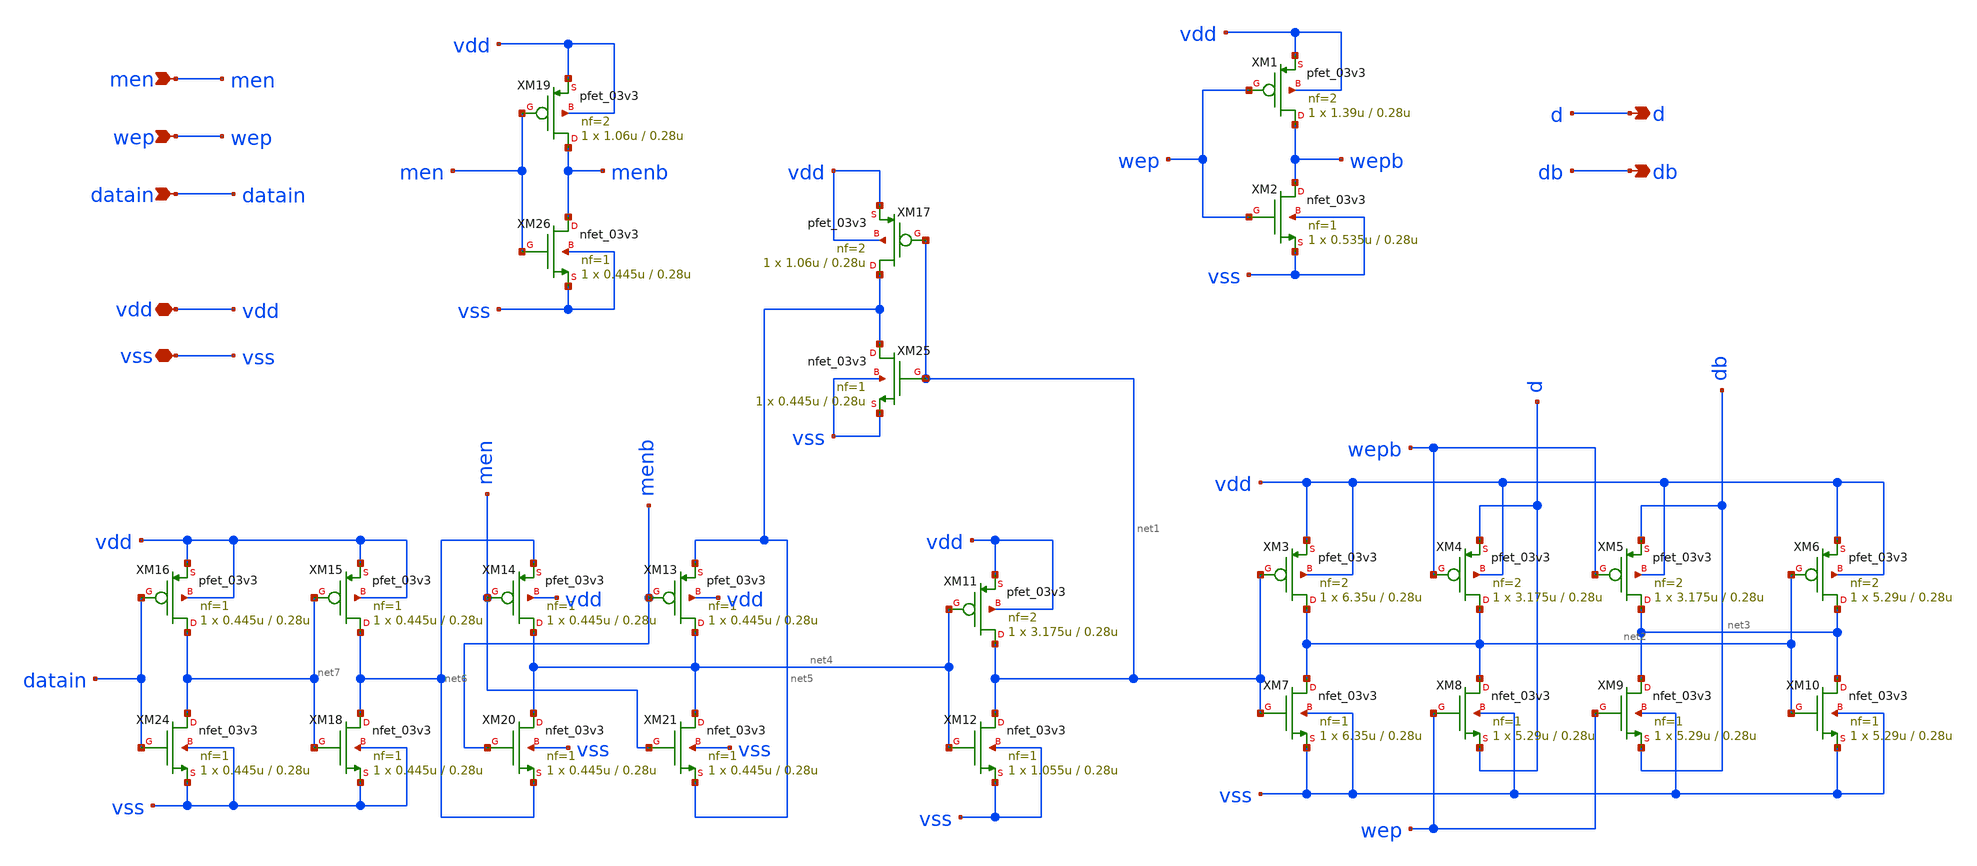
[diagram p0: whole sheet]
** sch_path: cells/gf180mcu_ocd_ip_sram__sram512x8m8wm1/xschem/din_3v512x8m81.sch
**.subckt din_3v512x8m81 men wep datain d db vdd vss
*.ipin men
*.ipin wep
*.ipin datain
*.opin d
*.opin db
*.iopin vdd
*.iopin vss
XM1 wepb wep vdd vdd pfet_03v3 L=0.28u W=1.39u nf=2 ad='int((nf+1)/2) * W/nf * 0.18u' as='int((nf+2)/2) * W/nf * 0.18u'
+ pd='2*int((nf+1)/2) * (W/nf + 0.18u)' ps='2*int((nf+2)/2) * (W/nf + 0.18u)' nrd='0.18u / W' nrs='0.18u / W'
+ sa=0 sb=0 sd=0 m=1
XM2 wepb wep vss vss nfet_03v3 L=0.28u W=0.535u nf=1 ad='int((nf+1)/2) * W/nf * 0.18u' as='int((nf+2)/2) * W/nf * 0.18u'
+ pd='2*int((nf+1)/2) * (W/nf + 0.18u)' ps='2*int((nf+2)/2) * (W/nf + 0.18u)' nrd='0.18u / W' nrs='0.18u / W'
+ sa=0 sb=0 sd=0 m=1
XM3 net2 net1 vdd vdd pfet_03v3 L=0.28u W=6.35u nf=2 ad='int((nf+1)/2) * W/nf * 0.18u' as='int((nf+2)/2) * W/nf * 0.18u'
+ pd='2*int((nf+1)/2) * (W/nf + 0.18u)' ps='2*int((nf+2)/2) * (W/nf + 0.18u)' nrd='0.18u / W' nrs='0.18u / W'
+ sa=0 sb=0 sd=0 m=1
XM4 net2 wepb d vdd pfet_03v3 L=0.28u W=3.175u nf=2 ad='int((nf+1)/2) * W/nf * 0.18u' as='int((nf+2)/2) * W/nf * 0.18u'
+ pd='2*int((nf+1)/2) * (W/nf + 0.18u)' ps='2*int((nf+2)/2) * (W/nf + 0.18u)' nrd='0.18u / W' nrs='0.18u / W'
+ sa=0 sb=0 sd=0 m=1
XM5 net3 wepb db vdd pfet_03v3 L=0.28u W=3.175u nf=2 ad='int((nf+1)/2) * W/nf * 0.18u' as='int((nf+2)/2) * W/nf * 0.18u'
+ pd='2*int((nf+1)/2) * (W/nf + 0.18u)' ps='2*int((nf+2)/2) * (W/nf + 0.18u)' nrd='0.18u / W' nrs='0.18u / W'
+ sa=0 sb=0 sd=0 m=1
XM6 net3 net2 vdd vdd pfet_03v3 L=0.28u W=5.29u nf=2 ad='int((nf+1)/2) * W/nf * 0.18u' as='int((nf+2)/2) * W/nf * 0.18u'
+ pd='2*int((nf+1)/2) * (W/nf + 0.18u)' ps='2*int((nf+2)/2) * (W/nf + 0.18u)' nrd='0.18u / W' nrs='0.18u / W'
+ sa=0 sb=0 sd=0 m=1
XM7 net2 net1 vss vss nfet_03v3 L=0.28u W=6.35u nf=1 ad='int((nf+1)/2) * W/nf * 0.18u' as='int((nf+2)/2) * W/nf * 0.18u'
+ pd='2*int((nf+1)/2) * (W/nf + 0.18u)' ps='2*int((nf+2)/2) * (W/nf + 0.18u)' nrd='0.18u / W' nrs='0.18u / W'
+ sa=0 sb=0 sd=0 m=1
XM8 net2 wep d vss nfet_03v3 L=0.28u W=5.29u nf=1 ad='int((nf+1)/2) * W/nf * 0.18u' as='int((nf+2)/2) * W/nf * 0.18u'
+ pd='2*int((nf+1)/2) * (W/nf + 0.18u)' ps='2*int((nf+2)/2) * (W/nf + 0.18u)' nrd='0.18u / W' nrs='0.18u / W'
+ sa=0 sb=0 sd=0 m=1
XM9 net3 wep db vss nfet_03v3 L=0.28u W=5.29u nf=1 ad='int((nf+1)/2) * W/nf * 0.18u' as='int((nf+2)/2) * W/nf * 0.18u'
+ pd='2*int((nf+1)/2) * (W/nf + 0.18u)' ps='2*int((nf+2)/2) * (W/nf + 0.18u)' nrd='0.18u / W' nrs='0.18u / W'
+ sa=0 sb=0 sd=0 m=1
XM10 net3 net2 vss vss nfet_03v3 L=0.28u W=5.29u nf=1 ad='int((nf+1)/2) * W/nf * 0.18u' as='int((nf+2)/2) * W/nf * 0.18u'
+ pd='2*int((nf+1)/2) * (W/nf + 0.18u)' ps='2*int((nf+2)/2) * (W/nf + 0.18u)' nrd='0.18u / W' nrs='0.18u / W'
+ sa=0 sb=0 sd=0 m=1
XM11 net1 net4 vdd vdd pfet_03v3 L=0.28u W=3.175u nf=2 ad='int((nf+1)/2) * W/nf * 0.18u' as='int((nf+2)/2) * W/nf * 0.18u'
+ pd='2*int((nf+1)/2) * (W/nf + 0.18u)' ps='2*int((nf+2)/2) * (W/nf + 0.18u)' nrd='0.18u / W' nrs='0.18u / W'
+ sa=0 sb=0 sd=0 m=1
XM12 net1 net4 vss vss nfet_03v3 L=0.28u W=1.055u nf=1 ad='int((nf+1)/2) * W/nf * 0.18u' as='int((nf+2)/2) * W/nf * 0.18u'
+ pd='2*int((nf+1)/2) * (W/nf + 0.18u)' ps='2*int((nf+2)/2) * (W/nf + 0.18u)' nrd='0.18u / W' nrs='0.18u / W'
+ sa=0 sb=0 sd=0 m=1
XM13 net4 menb net5 vdd pfet_03v3 L=0.28u W=0.445u nf=1 ad='int((nf+1)/2) * W/nf * 0.18u' as='int((nf+2)/2) * W/nf * 0.18u'
+ pd='2*int((nf+1)/2) * (W/nf + 0.18u)' ps='2*int((nf+2)/2) * (W/nf + 0.18u)' nrd='0.18u / W' nrs='0.18u / W'
+ sa=0 sb=0 sd=0 m=1
XM14 net4 men net6 vdd pfet_03v3 L=0.28u W=0.445u nf=1 ad='int((nf+1)/2) * W/nf * 0.18u' as='int((nf+2)/2) * W/nf * 0.18u'
+ pd='2*int((nf+1)/2) * (W/nf + 0.18u)' ps='2*int((nf+2)/2) * (W/nf + 0.18u)' nrd='0.18u / W' nrs='0.18u / W'
+ sa=0 sb=0 sd=0 m=1
XM15 net6 net7 vdd vdd pfet_03v3 L=0.28u W=0.445u nf=1 ad='int((nf+1)/2) * W/nf * 0.18u' as='int((nf+2)/2) * W/nf * 0.18u'
+ pd='2*int((nf+1)/2) * (W/nf + 0.18u)' ps='2*int((nf+2)/2) * (W/nf + 0.18u)' nrd='0.18u / W' nrs='0.18u / W'
+ sa=0 sb=0 sd=0 m=1
XM16 net7 datain vdd vdd pfet_03v3 L=0.28u W=0.445u nf=1 ad='int((nf+1)/2) * W/nf * 0.18u' as='int((nf+2)/2) * W/nf * 0.18u'
+ pd='2*int((nf+1)/2) * (W/nf + 0.18u)' ps='2*int((nf+2)/2) * (W/nf + 0.18u)' nrd='0.18u / W' nrs='0.18u / W'
+ sa=0 sb=0 sd=0 m=1
XM17 net5 net1 vdd vdd pfet_03v3 L=0.28u W=1.06u nf=2 ad='int((nf+1)/2) * W/nf * 0.18u' as='int((nf+2)/2) * W/nf * 0.18u'
+ pd='2*int((nf+1)/2) * (W/nf + 0.18u)' ps='2*int((nf+2)/2) * (W/nf + 0.18u)' nrd='0.18u / W' nrs='0.18u / W'
+ sa=0 sb=0 sd=0 m=1
XM19 menb men vdd vdd pfet_03v3 L=0.28u W=1.06u nf=2 ad='int((nf+1)/2) * W/nf * 0.18u' as='int((nf+2)/2) * W/nf * 0.18u'
+ pd='2*int((nf+1)/2) * (W/nf + 0.18u)' ps='2*int((nf+2)/2) * (W/nf + 0.18u)' nrd='0.18u / W' nrs='0.18u / W'
+ sa=0 sb=0 sd=0 m=1
XM24 net7 datain vss vss nfet_03v3 L=0.28u W=0.445u nf=1 ad='int((nf+1)/2) * W/nf * 0.18u' as='int((nf+2)/2) * W/nf * 0.18u'
+ pd='2*int((nf+1)/2) * (W/nf + 0.18u)' ps='2*int((nf+2)/2) * (W/nf + 0.18u)' nrd='0.18u / W' nrs='0.18u / W'
+ sa=0 sb=0 sd=0 m=1
XM25 net5 net1 vss vss nfet_03v3 L=0.28u W=0.445u nf=1 ad='int((nf+1)/2) * W/nf * 0.18u' as='int((nf+2)/2) * W/nf * 0.18u'
+ pd='2*int((nf+1)/2) * (W/nf + 0.18u)' ps='2*int((nf+2)/2) * (W/nf + 0.18u)' nrd='0.18u / W' nrs='0.18u / W'
+ sa=0 sb=0 sd=0 m=1
XM26 menb men vss vss nfet_03v3 L=0.28u W=0.445u nf=1 ad='int((nf+1)/2) * W/nf * 0.18u' as='int((nf+2)/2) * W/nf * 0.18u'
+ pd='2*int((nf+1)/2) * (W/nf + 0.18u)' ps='2*int((nf+2)/2) * (W/nf + 0.18u)' nrd='0.18u / W' nrs='0.18u / W'
+ sa=0 sb=0 sd=0 m=1
XM18 net6 net7 vss vss nfet_03v3 L=0.28u W=0.445u nf=1 ad='int((nf+1)/2) * W/nf * 0.18u' as='int((nf+2)/2) * W/nf * 0.18u'
+ pd='2*int((nf+1)/2) * (W/nf + 0.18u)' ps='2*int((nf+2)/2) * (W/nf + 0.18u)' nrd='0.18u / W' nrs='0.18u / W'
+ sa=0 sb=0 sd=0 m=1
XM20 net4 menb net6 vss nfet_03v3 L=0.28u W=0.445u nf=1 ad='int((nf+1)/2) * W/nf * 0.18u' as='int((nf+2)/2) * W/nf * 0.18u'
+ pd='2*int((nf+1)/2) * (W/nf + 0.18u)' ps='2*int((nf+2)/2) * (W/nf + 0.18u)' nrd='0.18u / W' nrs='0.18u / W'
+ sa=0 sb=0 sd=0 m=1
XM21 net4 men net5 vss nfet_03v3 L=0.28u W=0.445u nf=1 ad='int((nf+1)/2) * W/nf * 0.18u' as='int((nf+2)/2) * W/nf * 0.18u'
+ pd='2*int((nf+1)/2) * (W/nf + 0.18u)' ps='2*int((nf+2)/2) * (W/nf + 0.18u)' nrd='0.18u / W' nrs='0.18u / W'
+ sa=0 sb=0 sd=0 m=1
**.ends
.end
